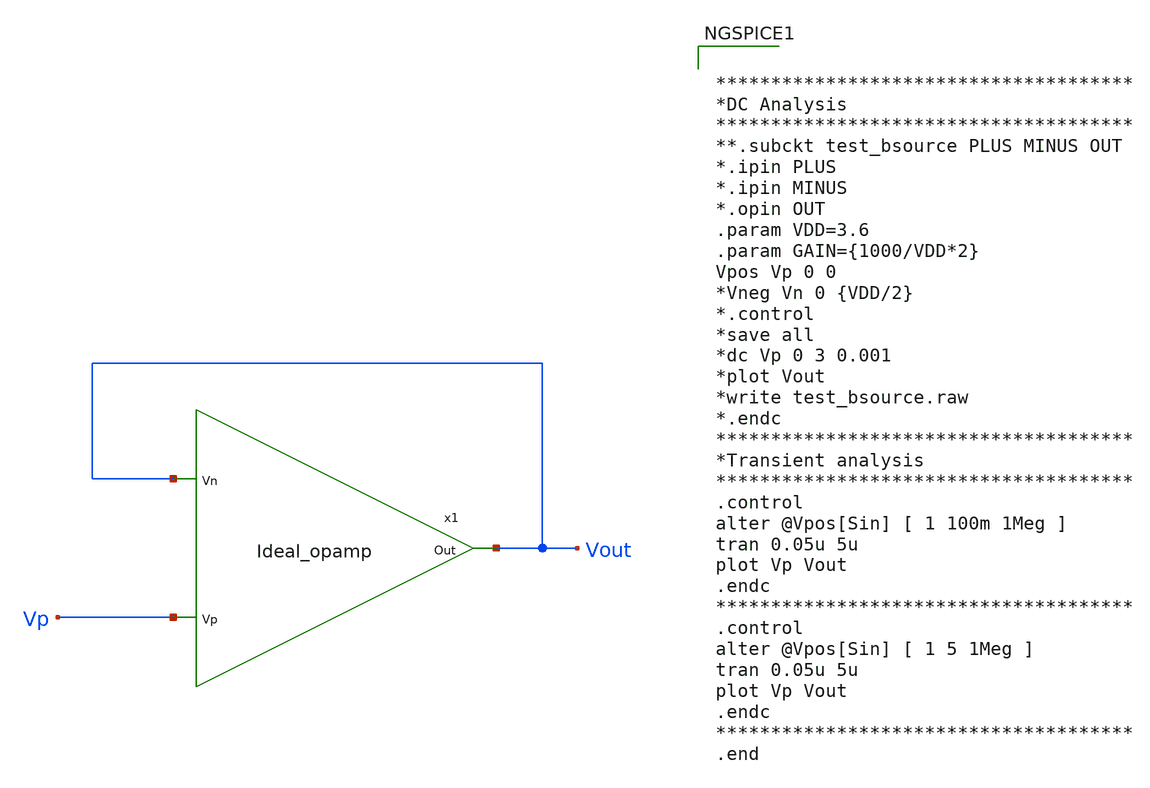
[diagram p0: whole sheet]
** sch_path: Analog_Blocks/OTA/Testbench/Ideal_opamp/test_Ideal_Opamp.sch
**.subckt test_Ideal_Opamp
x1 Vp Vout Vout Ideal_opamp
**** begin user architecture code


.param mc_mm_switch=0
.param mc_pr_switch=0
.include ~/mabrains/Analog_blocks/models/sky130A/libs.ref/sky130_fd_pr/spice/sky130_fd_pr__nfet_01v8__tt.corner.spice
.include ~/mabrains/Analog_blocks/models/sky130A/libs.ref/sky130_fd_pr/spice/sky130_fd_pr__nfet_01v8_lvt__tt.corner.spice
.include ~/mabrains/Analog_blocks/models/sky130A/libs.ref/sky130_fd_pr/spice/sky130_fd_pr__pfet_01v8__tt.corner.spice
.include ~/mabrains/Analog_blocks/models/sky130A/libs.ref/sky130_fd_pr/spice/sky130_fd_pr__nfet_03v3_nvt__tt.corner.spice
.include ~/mabrains/Analog_blocks/models/sky130A/libs.ref/sky130_fd_pr/spice/sky130_fd_pr__nfet_05v0_nvt__tt.corner.spice
.include ~/mabrains/Analog_blocks/models/sky130A/libs.ref/sky130_fd_pr/spice/sky130_fd_pr__esd_nfet_01v8__tt.corner.spice
.include ~/mabrains/Analog_blocks/models/sky130A/libs.ref/sky130_fd_pr/spice/sky130_fd_pr__pfet_01v8_lvt__tt.corner.spice
.include ~/mabrains/Analog_blocks/models/sky130A/libs.ref/sky130_fd_pr/spice/sky130_fd_pr__pfet_01v8_hvt__tt.corner.spice
.include ~/mabrains/Analog_blocks/models/sky130A/libs.ref/sky130_fd_pr/spice/sky130_fd_pr__esd_pfet_g5v0d10v5__tt.corner.spice
.include ~/mabrains/Analog_blocks/models/sky130A/libs.ref/sky130_fd_pr/spice/sky130_fd_pr__pfet_g5v0d10v5__tt.corner.spice
.include ~/mabrains/Analog_blocks/models/sky130A/libs.ref/sky130_fd_pr/spice/sky130_fd_pr__pfet_g5v0d16v0__tt.corner.spice
.include ~/mabrains/Analog_blocks/models/sky130A/libs.ref/sky130_fd_pr/spice/sky130_fd_pr__nfet_g5v0d10v5__tt.corner.spice
.include ~/mabrains/Analog_blocks/models/sky130A/libs.ref/sky130_fd_pr/spice/sky130_fd_pr__nfet_g5v0d16v0__tt_discrete.corner.spice
.include ~/mabrains/Analog_blocks/models/sky130A/libs.ref/sky130_fd_pr/spice/sky130_fd_pr__esd_nfet_g5v0d10v5__tt.corner.spice
.include ~/mabrains/Analog_blocks/models/sky130A/libs.ref/sky130_fd_pr/spice/sky130_fd_pr__nfet_20v0__tt_discrete.corner.spice
.include ~/mabrains/Analog_blocks/models/sky130A/libs.ref/sky130_fd_pr/spice/sky130_fd_pr__pfet_20v0__tt_discrete.corner.spice
.include ~/mabrains/Analog_blocks/models/sky130A/libs.tech/ngspice/corners/tt/nonfet.spice
* Mismatch parameters
.include ~/mabrains/Analog_blocks/models/sky130A/libs.ref/sky130_fd_pr/spice/sky130_fd_pr__nfet_01v8__mismatch.corner.spice
.include ~/mabrains/Analog_blocks/models/sky130A/libs.ref/sky130_fd_pr/spice/sky130_fd_pr__pfet_01v8__mismatch.corner.spice
.include ~/mabrains/Analog_blocks/models/sky130A/libs.ref/sky130_fd_pr/spice/sky130_fd_pr__nfet_01v8_lvt__mismatch.corner.spice
.include ~/mabrains/Analog_blocks/models/sky130A/libs.ref/sky130_fd_pr/spice/sky130_fd_pr__pfet_01v8_lvt__mismatch.corner.spice
.include ~/mabrains/Analog_blocks/models/sky130A/libs.ref/sky130_fd_pr/spice/sky130_fd_pr__pfet_01v8_hvt__mismatch.corner.spice
.include ~/mabrains/Analog_blocks/models/sky130A/libs.ref/sky130_fd_pr/spice/sky130_fd_pr__nfet_g5v0d10v5__mismatch.corner.spice
.include ~/mabrains/Analog_blocks/models/sky130A/libs.ref/sky130_fd_pr/spice/sky130_fd_pr__pfet_g5v0d10v5__mismatch.corner.spice
.include ~/mabrains/Analog_blocks/models/sky130A/libs.ref/sky130_fd_pr/spice/sky130_fd_pr__nfet_05v0_nvt__mismatch.corner.spice
.include ~/mabrains/Analog_blocks/models/sky130A/libs.ref/sky130_fd_pr/spice/sky130_fd_pr__nfet_03v3_nvt__mismatch.corner.spice
* Resistor/Capacitor
.include ~/mabrains/Analog_blocks/models/sky130A/libs.tech/ngspice/r+c/res_typical__cap_typical.spice
.include ~/mabrains/Analog_blocks/models/sky130A/libs.tech/ngspice/r+c/res_typical__cap_typical__lin.spice
* Special cells
.include ~/mabrains/Analog_blocks/models/sky130A/libs.tech/ngspice/corners/tt/specialized_cells.spice
* All models
.include ~/mabrains/Analog_blocks/models/sky130A/libs.tech/ngspice/all.spice
* Corner
.include ~/mabrains/Analog_blocks/models/sky130A/libs.tech/ngspice/corners/tt/rf.spice





**************************************
*DC Analysis
**************************************
**.subckt test_bsource PLUS MINUS OUT
*.ipin PLUS
*.ipin MINUS
*.opin OUT
.param VDD=3.6
.param GAIN={1000/VDD*2}
Vpos Vp 0 0
*Vneg Vn 0 {VDD/2}
*.control
*save all
*dc Vp 0 3 0.001
*plot Vout
*write test_bsource.raw
*.endc
**************************************
*Transient analysis
**************************************
.control
alter @Vpos[Sin] [ 1 100m 1Meg ]
tran 0.05u 5u
plot Vp Vout
.endc
**************************************
.control
alter @Vpos[Sin] [ 1 5 1Meg ]
tran 0.05u 5u
plot Vp Vout
.endc
**************************************
.end


**** end user architecture code
**.ends

* expanding   symbol:
*+  /home/eslam/mabrains/Analog_blocks/Analog_Blocks/OTA/Schematic/Ideal_opamp/Ideal_opamp.sym # of pins=3
** sym_path: Analog_blocks/Analog_Blocks/OTA/Schematic/Ideal_opamp/Ideal_opamp.sym
** sch_path: Analog_blocks/Analog_Blocks/OTA/Schematic/Ideal_opamp/Ideal_opamp.sch
.subckt Ideal_opamp Vp Out Vn
*.ipin Vp
*.ipin Vn
*.opin Out
V1 Vp PLUS_I 0
.save i(v1)
V2 Vn MINUS_I 0
.save i(v2)
B1 Out 0 V = 'VDD/2*(1+tanh(GAIN*(V(PLUS_I)-V(MINUS_I))))'
.ends

.end
